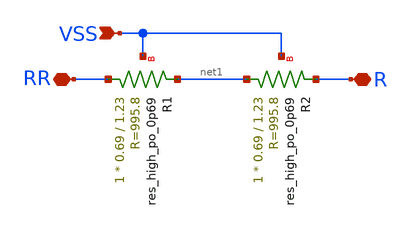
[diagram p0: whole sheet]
** sch_path: Res_2K_v1.sch
**.subckt Res_2K_v1 R RR VSS
*.iopin R
*.iopin RR
*.ipin VSS
XR1 RR net1 VSS sky130_fd_pr__res_high_po_0p69 L=1.23 mult=1 m=1
XR2 net1 R VSS sky130_fd_pr__res_high_po_0p69 L=1.23 mult=1 m=1
**.ends
.end
